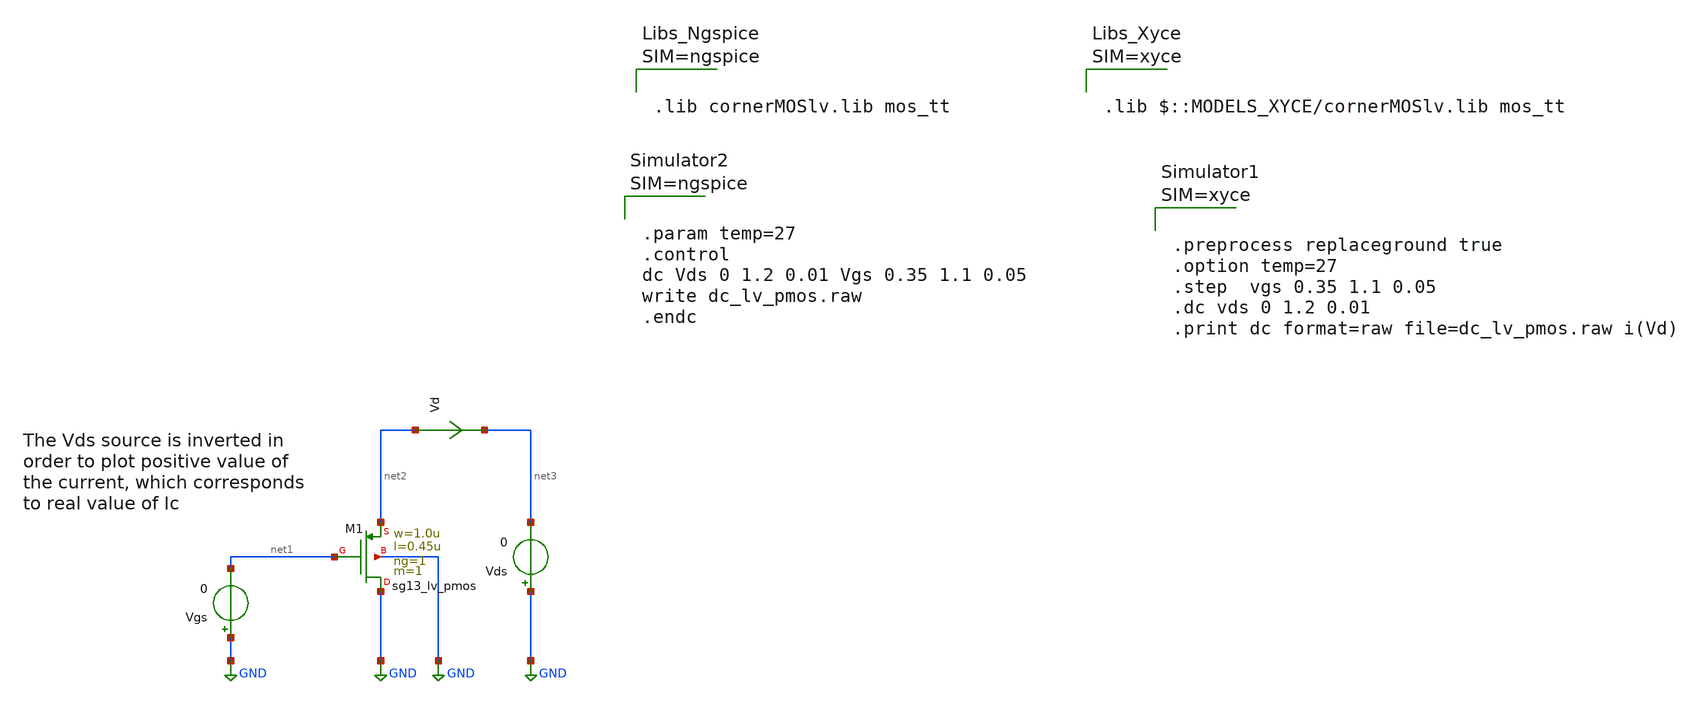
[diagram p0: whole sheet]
** sch_path: ihp-sg13g2/libs.tech/xschem/sg13g2_tests_xyce/dc_lv_pmos.sch
* Copyright 2023 IHP PDK Authors
**.subckt dc_lv_pmos
Vgs GND net1 0
Vds GND net3 0
XM1 GND net1 net2 GND sg13_lv_pmos w=1.0u l=0.45u ng=1 m=1 mm_ok=1
Vd net2 net3 0
.save i(vd)
**** begin user architecture code









.lib cornerMOSlv.lib mos_tt






.param temp=27
.control
dc Vds 0 1.2 0.01 Vgs 0.35 1.1 0.05
write dc_lv_pmos.raw
.endc



**** end user architecture code
**.ends
.GLOBAL GND
.end
